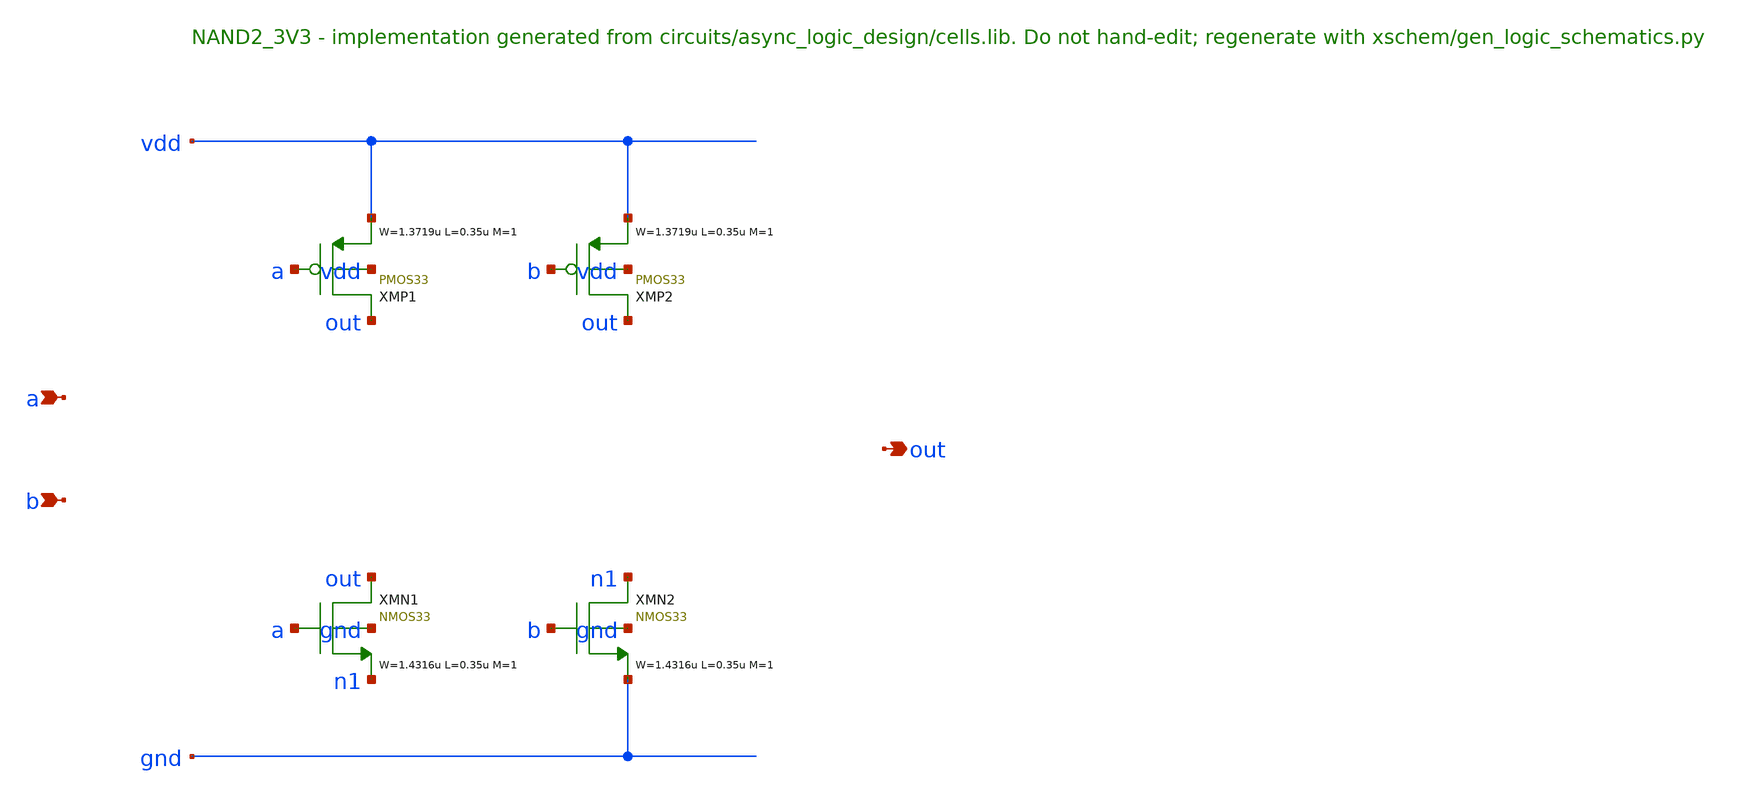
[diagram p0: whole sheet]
** sch_path: xschem/logic/NAND2_3V3.sch
**.subckt NAND2_3V3 a b out
*.ipin a
*.ipin b
*.opin out
XMP1 out a vdd vdd PMOS33 W=1.3719u L=0.35u M=1 MM_SIGMA=0
XMP2 out b vdd vdd PMOS33 W=1.3719u L=0.35u M=1 MM_SIGMA=0
XMN1 out a n1 gnd NMOS33 W=1.4316u L=0.35u M=1 MM_SIGMA=0
XMN2 n1 b gnd gnd NMOS33 W=1.4316u L=0.35u M=1 MM_SIGMA=0
**.ends
.end
